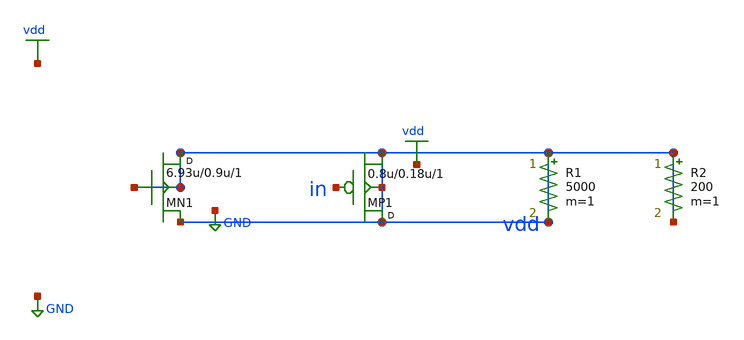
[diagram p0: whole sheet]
** sch_path: synthetic/generated/0042_synthetic.sch
**.subckt 0042_synthetic
MN1 vdd vdd vdd vdd nmos w=6.93u l=0.9u m=1
MP1 vdd in vdd vdd pmos w=0.8u l=0.18u m=1
R1 vdd vdd 5000 m=1
R2 vdd vdd 200 m=1
**.ends
.GLOBAL GND
.GLOBAL vdd
.end
